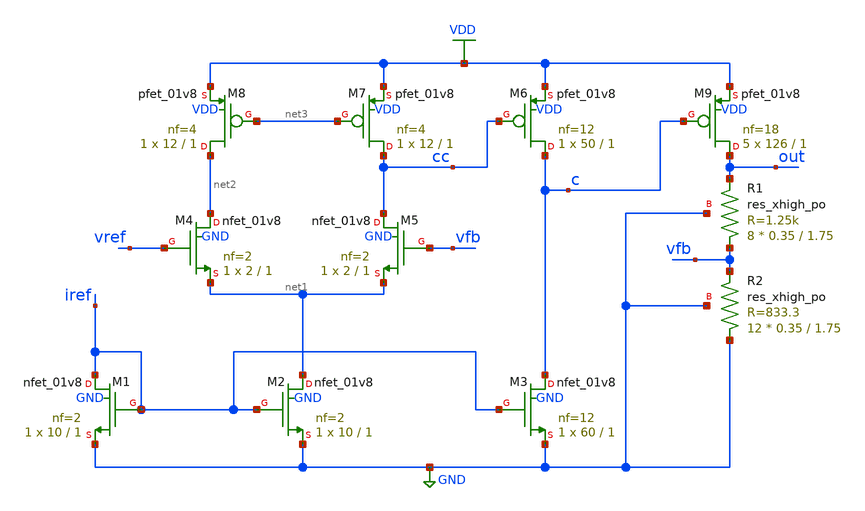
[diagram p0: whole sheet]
** sch_path: netlists/ldo.sch
**.subckt ldo
XM1 iref iref GND GND sky130_fd_pr__nfet_01v8 L=1 W=10 nf=2 ad='int((nf+1)/2) * W/nf * 0.29' as='int((nf+2)/2) * W/nf * 0.29'
+ pd='2*int((nf+1)/2) * (W/nf + 0.29)' ps='2*int((nf+2)/2) * (W/nf + 0.29)' nrd='0.29 / W' nrs='0.29 / W'
+ sa=0 sb=0 sd=0 mult=1 m=1
XM2 net1 iref GND GND sky130_fd_pr__nfet_01v8 L=1 W=10 nf=2 ad='int((nf+1)/2) * W/nf * 0.29' as='int((nf+2)/2) * W/nf * 0.29'
+ pd='2*int((nf+1)/2) * (W/nf + 0.29)' ps='2*int((nf+2)/2) * (W/nf + 0.29)' nrd='0.29 / W' nrs='0.29 / W'
+ sa=0 sb=0 sd=0 mult=1 m=1
XM3 c iref GND GND sky130_fd_pr__nfet_01v8 L=1 W=60 nf=12 ad='int((nf+1)/2) * W/nf * 0.29' as='int((nf+2)/2) * W/nf * 0.29'
+ pd='2*int((nf+1)/2) * (W/nf + 0.29)' ps='2*int((nf+2)/2) * (W/nf + 0.29)' nrd='0.29 / W' nrs='0.29 / W'
+ sa=0 sb=0 sd=0 mult=1 m=1
XM4 net2 vref net1 GND sky130_fd_pr__nfet_01v8 L=1 W=2 nf=2 ad='int((nf+1)/2) * W/nf * 0.29' as='int((nf+2)/2) * W/nf * 0.29'
+ pd='2*int((nf+1)/2) * (W/nf + 0.29)' ps='2*int((nf+2)/2) * (W/nf + 0.29)' nrd='0.29 / W' nrs='0.29 / W'
+ sa=0 sb=0 sd=0 mult=1 m=1
XM5 cc vfb net1 GND sky130_fd_pr__nfet_01v8 L=1 W=2 nf=2 ad='int((nf+1)/2) * W/nf * 0.29' as='int((nf+2)/2) * W/nf * 0.29'
+ pd='2*int((nf+1)/2) * (W/nf + 0.29)' ps='2*int((nf+2)/2) * (W/nf + 0.29)' nrd='0.29 / W' nrs='0.29 / W'
+ sa=0 sb=0 sd=0 mult=1 m=1
XM6 c cc VDD VDD sky130_fd_pr__pfet_01v8 L=1 W=50 nf=12 ad='int((nf+1)/2) * W/nf * 0.29' as='int((nf+2)/2) * W/nf * 0.29'
+ pd='2*int((nf+1)/2) * (W/nf + 0.29)' ps='2*int((nf+2)/2) * (W/nf + 0.29)' nrd='0.29 / W' nrs='0.29 / W'
+ sa=0 sb=0 sd=0 mult=1 m=1
XM7 cc net3 VDD VDD sky130_fd_pr__pfet_01v8 L=1 W=12 nf=4 ad='int((nf+1)/2) * W/nf * 0.29' as='int((nf+2)/2) * W/nf * 0.29'
+ pd='2*int((nf+1)/2) * (W/nf + 0.29)' ps='2*int((nf+2)/2) * (W/nf + 0.29)' nrd='0.29 / W' nrs='0.29 / W'
+ sa=0 sb=0 sd=0 mult=1 m=1
XM8 net2 net3 VDD VDD sky130_fd_pr__pfet_01v8 L=1 W=12 nf=4 ad='int((nf+1)/2) * W/nf * 0.29' as='int((nf+2)/2) * W/nf * 0.29'
+ pd='2*int((nf+1)/2) * (W/nf + 0.29)' ps='2*int((nf+2)/2) * (W/nf + 0.29)' nrd='0.29 / W' nrs='0.29 / W'
+ sa=0 sb=0 sd=0 mult=1 m=1
XM9 out c VDD VDD sky130_fd_pr__pfet_01v8 L=1 W=126 nf=18 ad='int((nf+1)/2) * W/nf * 0.29' as='int((nf+2)/2) * W/nf * 0.29'
+ pd='2*int((nf+1)/2) * (W/nf + 0.29)' ps='2*int((nf+2)/2) * (W/nf + 0.29)' nrd='0.29 / W' nrs='0.29 / W'
+ sa=0 sb=0 sd=0 mult=5 m=5
XR1 vfb out GND sky130_fd_pr__res_xhigh_po W=0.35 L=1.75 mult=8 m=8
XR2 GND vfb GND sky130_fd_pr__res_xhigh_po W=0.35 L=1.75 mult=12 m=12
**.ends
.GLOBAL VDD
.GLOBAL GND
.end
